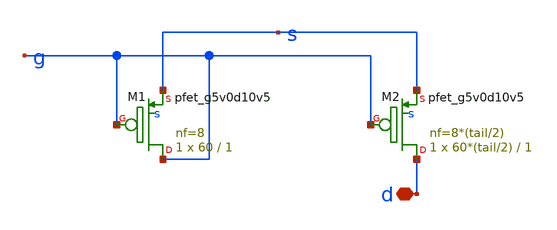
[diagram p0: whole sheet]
** sch_path: xschem/mosbius_lib/mosbius_ptail.sch
**.subckt mosbius_ptail d
*.iopin d
XM1 g g s s sky130_fd_pr__pfet_g5v0d10v5 L=1 W=60 nf=8 ad='int((nf+1)/2) * W/nf * 0.29' as='int((nf+2)/2) * W/nf * 0.29'
+ pd='2*int((nf+1)/2) * (W/nf + 0.29)' ps='2*int((nf+2)/2) * (W/nf + 0.29)' nrd='0.29 / W' nrs='0.29 / W'
+ sa=0 sb=0 sd=0 mult=1 m=1
XM2 d g s s sky130_fd_pr__pfet_g5v0d10v5 L=1 W=60*(tail/2) nf=8*(tail/2) ad='int((nf+1)/2) * W/nf * 0.29'
+ as='int((nf+2)/2) * W/nf * 0.29' pd='2*int((nf+1)/2) * (W/nf + 0.29)' ps='2*int((nf+2)/2) * (W/nf + 0.29)'
+ nrd='0.29 / W' nrs='0.29 / W' sa=0 sb=0 sd=0 mult=1 m=1
**.ends
.end
